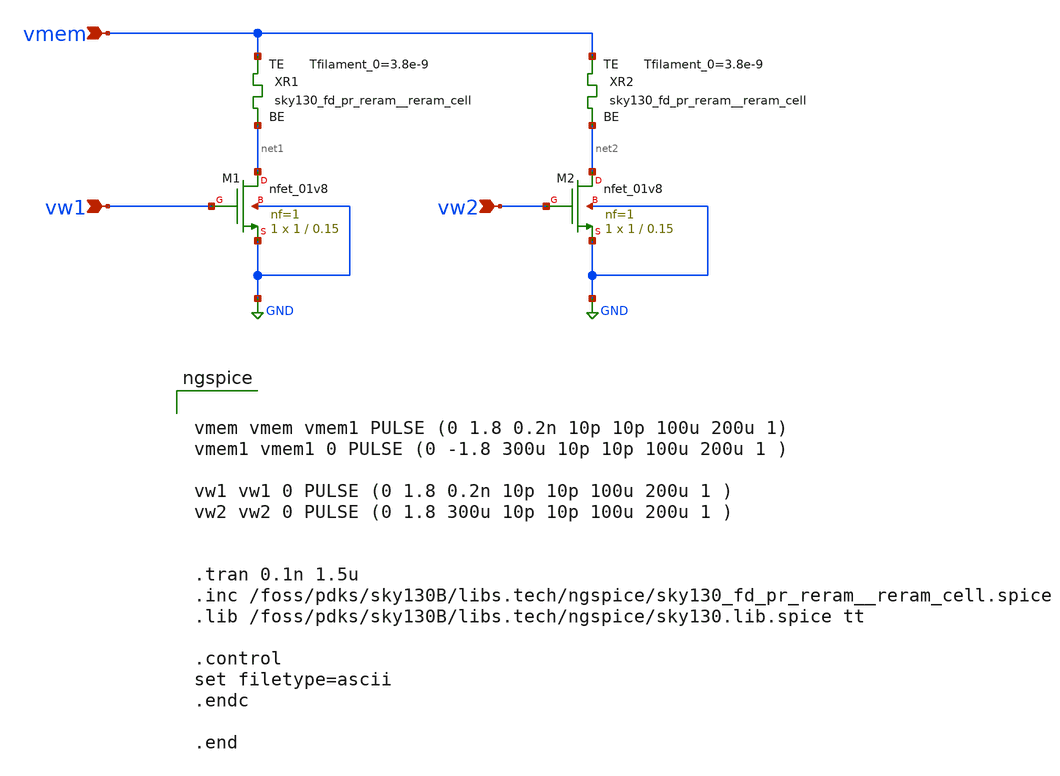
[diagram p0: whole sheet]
** sch_path: xschem/Func_2bit.sch
* StefanSchippers/xschem_sky130/sky130_fd_pr/reram.sym:
* Copyright 2021 Stefan Frederik Schippers
* Licensed under the Apache License, Version 2.0 (the "License");
**.subckt Func_2bit vmem vw1 vw2
*.ipin vmem
*.ipin vw1
*.ipin vw2
XM1 net1 vw1 GND GND sky130_fd_pr__nfet_01v8 L=0.15 W=1 nf=1 ad='int((nf+1)/2) * W/nf * 0.29' as='int((nf+2)/2) * W/nf * 0.29'
+ pd='2*int((nf+1)/2) * (W/nf + 0.29)' ps='2*int((nf+2)/2) * (W/nf + 0.29)' nrd='0.29 / W' nrs='0.29 / W'
+ sa=0 sb=0 sd=0 mult=1 m=1
XM2 net2 vw2 GND GND sky130_fd_pr__nfet_01v8 L=0.15 W=1 nf=1 ad='int((nf+1)/2) * W/nf * 0.29' as='int((nf+2)/2) * W/nf * 0.29'
+ pd='2*int((nf+1)/2) * (W/nf + 0.29)' ps='2*int((nf+2)/2) * (W/nf + 0.29)' nrd='0.29 / W' nrs='0.29 / W'
+ sa=0 sb=0 sd=0 mult=1 m=1
XR1 vmem net1 sky130_fd_pr_reram__reram_cell Tfilament_0=3.8e-9
XR2 vmem net2 sky130_fd_pr_reram__reram_cell Tfilament_0=3.8e-9
**** begin user architecture code


vmem vmem vmem1 PULSE (0 1.8 0.2n 10p 10p 100u 200u 1)
vmem1 vmem1 0 PULSE (0 -1.8 300u 10p 10p 100u 200u 1 )

vw1 vw1 0 PULSE (0 1.8 0.2n 10p 10p 100u 200u 1 )
vw2 vw2 0 PULSE (0 1.8 300u 10p 10p 100u 200u 1 )


.tran 0.1n 1.5u
.inc /foss/pdks/sky130B/libs.tech/ngspice/sky130_fd_pr_reram__reram_cell.spice
.lib /foss/pdks/sky130B/libs.tech/ngspice/sky130.lib.spice tt

.control
set filetype=ascii
.endc

.end


**** end user architecture code
**.ends
.GLOBAL GND
**** begin user architecture code

.subckt sky130_fd_pr_reram__reram_cell TE BE Tfilament_0=3.3e-9 area_ox=0.1024e-12
N1 TE BE nFilament sky130_fd_pr_reram__reram_model
.ic v(nFilament)={Tfilament_0*1.0e9}
.ends sky130_fd_pr_reram__reram_cell

.model sky130_fd_pr_reram__reram_model sky130_fd_pr_reram__reram_module  area_ox = 0.1024e-12  Tox =
+ 5.0  Tfilament_max = 4.9  Tfilament_min = 3.3  Eact_generation = 1.501  Eact_recombination  = 1.500
+  I_k1  = 6.140e-5  Tfilament_ref = 4.7249  V_ref = 0.430  velocity_k1 = 150  gamma_k0  = 16.5  gamma_k1
+  = -1.25  Temperature_0 = 300  C_thermal = 3.1825e-16  tau_thermal = 0.23e-9  t_step  = 1.0e-9
+  smoothing = 1e-7  Kclip = 200

.control
pre_osdi $SKYWATER_MODELS/sky130_fd_pr_reram__reram_module.osdi
.endc

**** end user architecture code
.end
